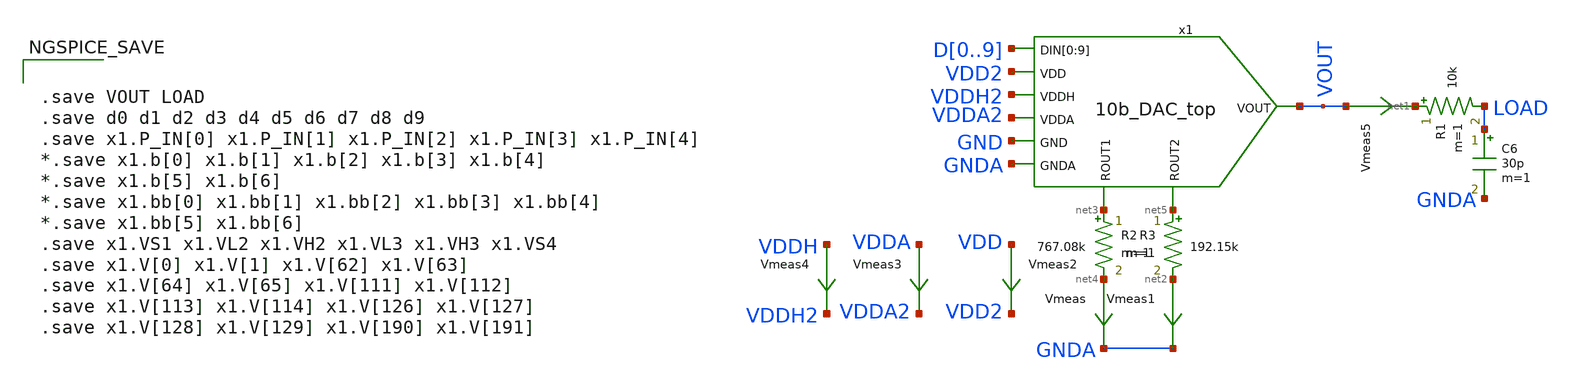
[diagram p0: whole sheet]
** sch_path: xschem/10b_DAC_dc-tb.sch
.lib $::SKYWATER_MODELS/sky130.lib.spice tt
.include $::SKYWATER_STDCELLS/sky130_fd_sc_hd.spice

**.subckt 10b_DAC_dc-tb
C6 LOAD GNDA 30p m=1
R1 net1 LOAD 10k m=1
Vmeas1 net2 GNDA 0
.save i(vmeas1)
R2 net3 net4 767.08k m=1
Vmeas net4 GNDA 0
.save i(vmeas)
R3 net5 net2 192.15k m=1
Vmeas2 VDD VDD2 0
.save i(vmeas2)
x1 D0 D1 D2 D3 D4 D5 D6 D7 D8 D9 VDD2 VDDH2 VDDA2 GND GNDA VOUT net3 net5 10b_DAC_top
Vmeas3 VDDA VDDA2 0
.save i(vmeas3)
Vmeas4 VDDH VDDH2 0
.save i(vmeas4)
Vmeas5 VOUT net1 0
.save i(vmeas5)
**** begin user architecture code


.save VOUT LOAD
.save d0 d1 d2 d3 d4 d5 d6 d7 d8 d9
.save x1.P_IN[0] x1.P_IN[1] x1.P_IN[2] x1.P_IN[3] x1.P_IN[4]
*.save x1.b[0] x1.b[1] x1.b[2] x1.b[3] x1.b[4]
*.save x1.b[5] x1.b[6]
*.save x1.bb[0] x1.bb[1] x1.bb[2] x1.bb[3] x1.bb[4]
*.save x1.bb[5] x1.bb[6]
.save x1.VS1 x1.VL2 x1.VH2 x1.VL3 x1.VH3 x1.VS4
.save x1.V[0] x1.V[1] x1.V[62] x1.V[63]
.save x1.V[64] x1.V[65] x1.V[111] x1.V[112]
.save x1.V[113] x1.V[114] x1.V[126] x1.V[127]
.save x1.V[128] x1.V[129] x1.V[190] x1.V[191]





  *.options wnflag=0 bypass=1
  .option wnflag=1
  .option safecurrents
  *.option klu
  .options solver=klu nomod
  .options method=trap rawfile=binary
  *.options reltol=1e-2 abstol=1e-12 chgtol=1e-12 vabstol=1u
  .nodeset all = 1
  *.nodeset V(VOUT) = 2.75 V(LOAD) = 2.75

  *nodeset 10 -> higher code
  *nodeset 1 -> Lower code
  ********************Static Voltage Sources***************************
  Vddh vddh gnd dc 5.5
  Vdd vdd gnd dc 1.8
  Vdda vdda gnd dc 5.5
  Vgnda gnda gnd dc 0

  Vdummy dummy gnd 0

  VHREF x1.V[191] GND 5.5
  VLREF x1.V[0] GND 0
  *****INPUT SIGNALS******
  .param xd0=0 xd1=0 xd2=0 xd3=0 xd4=0 xd5=0 xd6=0 xd7=0 xd8=0 xd9=0
  Vd0  d0  gnd {xd0}
  Vd1  d1  gnd {xd1}
  Vd2  d2  gnd {xd2}
  Vd3  d3  gnd {xd3}
  Vd4  d4  gnd {xd4}
  Vd5  d5  gnd {xd5}
  Vd6  d6  gnd {xd6}
  Vd7  d7  gnd {xd7}
  Vd8  d8  gnd {xd8}
  Vd9  d9  gnd {xd9}
  ********************Simulation Commands*****************************
  .control
     set num_threads=8
     *set appendwrite
     option numdgt=6
     set wr_singlescale
     set wr_vecnames

     let ndata=0

     compose low_to_high values 0 1.8
     compose high_to_low values 1.8 0

     foreach var9 $&low_to_high
       alter vd9 $var9

       foreach var8 $&low_to_high
         alter vd8 $var8

         foreach var7 $&low_to_high
           alter vd7 $var7

             foreach var6 $&low_to_high
             alter vd6 $var6

             foreach var5 $&low_to_high
             alter vd5 $var5

             foreach var4 $&low_to_high
             alter vd4 $var4

             foreach var3 $&low_to_high
             alter vd3 $var3

             foreach var2 $&low_to_high
             alter vd2 $var2

             foreach var1 $&low_to_high
             alter vd1 $var1

             foreach var0 $&low_to_high
             alter vd0 $var0

             dc vdummy 5 5 0.1
             let voutval= v(vout)
             let vloadval = v(load)

             let ir1 = i(vmeas)
             let ir2 = i(vmeas1)
             let ivdd = i(vmeas2)
             let ivdda = i(vmeas3)
             let ivddh = i(vmeas4)

             let vd0 = v(d0)
             let vd1 = v(d1)
             let vd2 = v(d2)
             let vd3 = v(d3)
             let vd4 = v(d4)
             let vd5 = v(d5)
             let vd6 = v(d6)
             let vd7 = v(d7)
             let vd8 = v(d8)
             let vd9 = v(d9)

             wrdata $THESIS_WS/simulations/dc_L_comp-tb.txt voutval vloadval ir1 ir2 ivdd ivdda
+ ivddh ndata vd9 vd8 vd7 vd6 vd5 vd4 vd3 vd2 vd1 vd0
             let ndata = ndata + 1
             set appendwrite
             unset set wr_vecnames
             destroy all

       end
       end
       end
       end
       end
       end
       end
       end
       end
     end

     set appendwrite=0
     reset
     *write 10b_DAC_dc-tb.raw

*    quit 0
  .endc



**** end user architecture code
**.ends
.end
